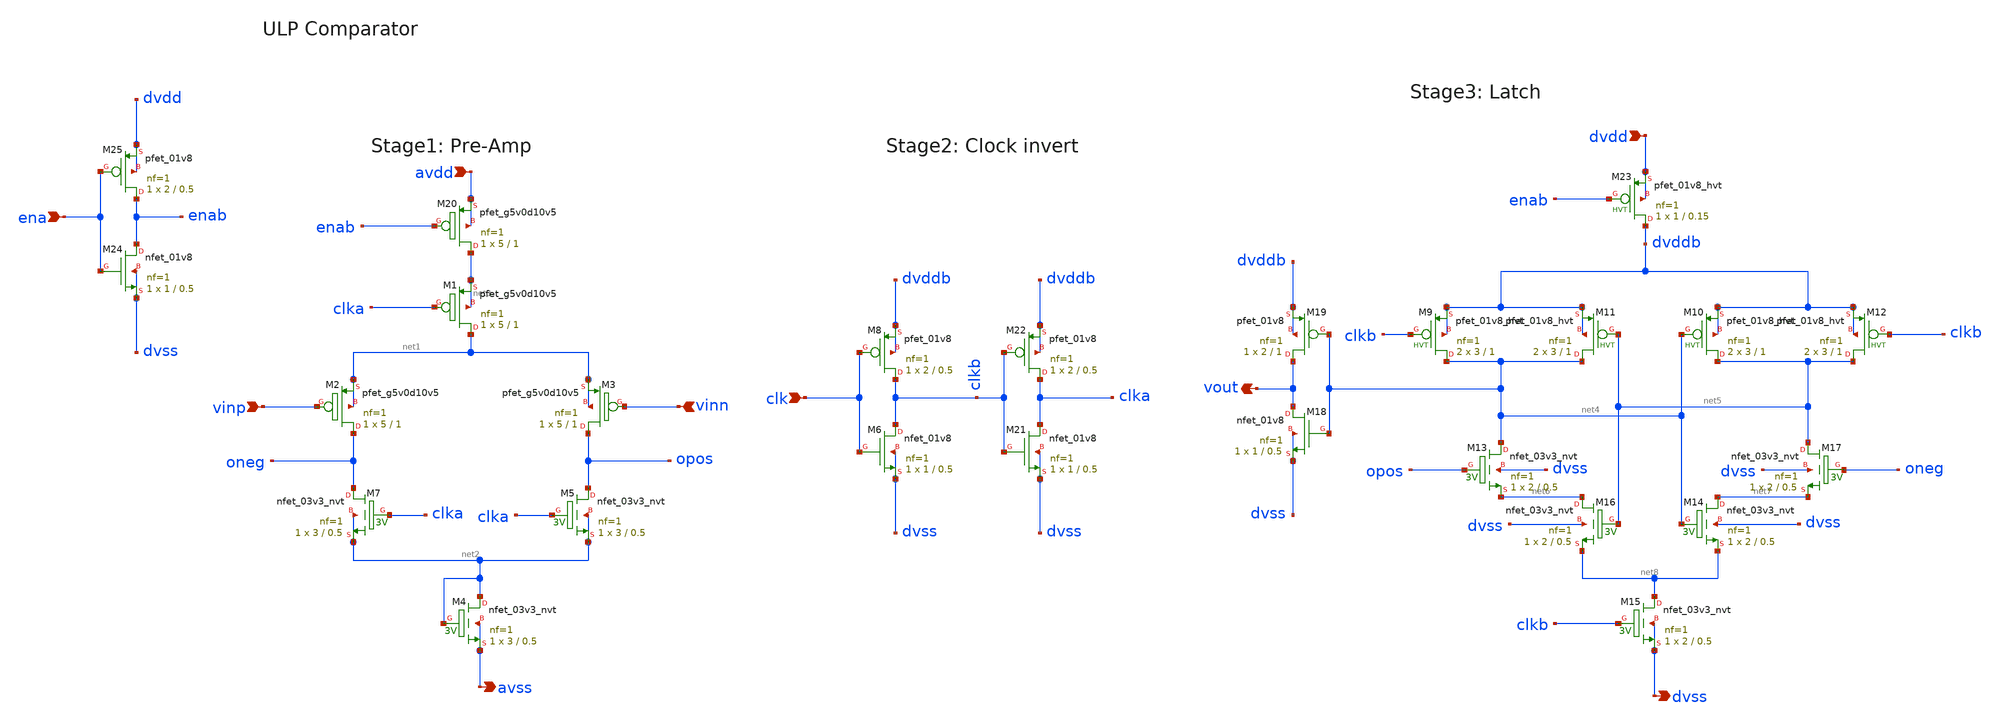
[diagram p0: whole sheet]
** sch_path: xschem/sky130_icrg_ip__ulpcomp2.sch
**.subckt sky130_icrg_ip__ulpcomp2 avdd vinp vinn avss vout dvss dvdd clk ena
*.ipin avdd
*.ipin vinp
*.ipin vinn
*.opin avss
*.opin vout
*.opin dvss
*.ipin dvdd
*.ipin clk
*.ipin ena
XM2 oneg vinp net1 net1 sky130_fd_pr__pfet_g5v0d10v5 L=1 W=5 nf=1 ad='int((nf+1)/2) * W/nf * 0.29' as='int((nf+2)/2) * W/nf * 0.29'
+ pd='2*int((nf+1)/2) * (W/nf + 0.29)' ps='2*int((nf+2)/2) * (W/nf + 0.29)' nrd='0.29 / W' nrs='0.29 / W'
+ sa=0 sb=0 sd=0 mult=1 m=1
XM3 opos vinn net1 net1 sky130_fd_pr__pfet_g5v0d10v5 L=1 W=5 nf=1 ad='int((nf+1)/2) * W/nf * 0.29' as='int((nf+2)/2) * W/nf * 0.29'
+ pd='2*int((nf+1)/2) * (W/nf + 0.29)' ps='2*int((nf+2)/2) * (W/nf + 0.29)' nrd='0.29 / W' nrs='0.29 / W'
+ sa=0 sb=0 sd=0 mult=1 m=1
XM7 oneg clka net2 net2 sky130_fd_pr__nfet_03v3_nvt L=0.5 W=3 nf=1 ad='int((nf+1)/2) * W/nf * 0.29' as='int((nf+2)/2) * W/nf * 0.29'
+ pd='2*int((nf+1)/2) * (W/nf + 0.29)' ps='2*int((nf+2)/2) * (W/nf + 0.29)' nrd='0.29 / W' nrs='0.29 / W'
+ sa=0 sb=0 sd=0 mult=1 m=1
XM5 opos clka net2 net2 sky130_fd_pr__nfet_03v3_nvt L=0.5 W=3 nf=1 ad='int((nf+1)/2) * W/nf * 0.29' as='int((nf+2)/2) * W/nf * 0.29'
+ pd='2*int((nf+1)/2) * (W/nf + 0.29)' ps='2*int((nf+2)/2) * (W/nf + 0.29)' nrd='0.29 / W' nrs='0.29 / W'
+ sa=0 sb=0 sd=0 mult=1 m=1
XM4 net2 net2 avss avss sky130_fd_pr__nfet_03v3_nvt L=0.5 W=3 nf=1 ad='int((nf+1)/2) * W/nf * 0.29' as='int((nf+2)/2) * W/nf * 0.29'
+ pd='2*int((nf+1)/2) * (W/nf + 0.29)' ps='2*int((nf+2)/2) * (W/nf + 0.29)' nrd='0.29 / W' nrs='0.29 / W'
+ sa=0 sb=0 sd=0 mult=1 m=1
XM18 vout net4 dvss dvss sky130_fd_pr__nfet_01v8 L=0.5 W=1 nf=1 ad='int((nf+1)/2) * W/nf * 0.29' as='int((nf+2)/2) * W/nf * 0.29'
+ pd='2*int((nf+1)/2) * (W/nf + 0.29)' ps='2*int((nf+2)/2) * (W/nf + 0.29)' nrd='0.29 / W' nrs='0.29 / W'
+ sa=0 sb=0 sd=0 mult=1 m=1
XM19 vout net4 dvddb dvddb sky130_fd_pr__pfet_01v8 L=1 W=2 nf=1 ad='int((nf+1)/2) * W/nf * 0.29' as='int((nf+2)/2) * W/nf * 0.29'
+ pd='2*int((nf+1)/2) * (W/nf + 0.29)' ps='2*int((nf+2)/2) * (W/nf + 0.29)' nrd='0.29 / W' nrs='0.29 / W'
+ sa=0 sb=0 sd=0 mult=1 m=1
XM22 clka clkb dvddb dvddb sky130_fd_pr__pfet_01v8 L=0.5 W=2 nf=1 ad='int((nf+1)/2) * W/nf * 0.29' as='int((nf+2)/2) * W/nf * 0.29'
+ pd='2*int((nf+1)/2) * (W/nf + 0.29)' ps='2*int((nf+2)/2) * (W/nf + 0.29)' nrd='0.29 / W' nrs='0.29 / W'
+ sa=0 sb=0 sd=0 mult=1 m=1
XM20 net3 enab avdd avdd sky130_fd_pr__pfet_g5v0d10v5 L=1 W=5 nf=1 ad='int((nf+1)/2) * W/nf * 0.29' as='int((nf+2)/2) * W/nf * 0.29'
+ pd='2*int((nf+1)/2) * (W/nf + 0.29)' ps='2*int((nf+2)/2) * (W/nf + 0.29)' nrd='0.29 / W' nrs='0.29 / W'
+ sa=0 sb=0 sd=0 mult=1 m=1
XM8 clkb clk dvddb dvddb sky130_fd_pr__pfet_01v8 L=0.5 W=2 nf=1 ad='int((nf+1)/2) * W/nf * 0.29' as='int((nf+2)/2) * W/nf * 0.29'
+ pd='2*int((nf+1)/2) * (W/nf + 0.29)' ps='2*int((nf+2)/2) * (W/nf + 0.29)' nrd='0.29 / W' nrs='0.29 / W'
+ sa=0 sb=0 sd=0 mult=1 m=1
XM25 enab ena dvdd dvdd sky130_fd_pr__pfet_01v8 L=0.5 W=2 nf=1 ad='int((nf+1)/2) * W/nf * 0.29' as='int((nf+2)/2) * W/nf * 0.29'
+ pd='2*int((nf+1)/2) * (W/nf + 0.29)' ps='2*int((nf+2)/2) * (W/nf + 0.29)' nrd='0.29 / W' nrs='0.29 / W'
+ sa=0 sb=0 sd=0 mult=1 m=1
XM13 net4 opos net6 dvss sky130_fd_pr__nfet_03v3_nvt L=0.5 W=2 nf=1 ad='int((nf+1)/2) * W/nf * 0.29'
+ as='int((nf+2)/2) * W/nf * 0.29' pd='2*int((nf+1)/2) * (W/nf + 0.29)' ps='2*int((nf+2)/2) * (W/nf + 0.29)'
+ nrd='0.29 / W' nrs='0.29 / W' sa=0 sb=0 sd=0 mult=1 m=1
XM14 net7 net4 net8 dvss sky130_fd_pr__nfet_03v3_nvt L=0.5 W=2 nf=1 ad='int((nf+1)/2) * W/nf * 0.29'
+ as='int((nf+2)/2) * W/nf * 0.29' pd='2*int((nf+1)/2) * (W/nf + 0.29)' ps='2*int((nf+2)/2) * (W/nf + 0.29)'
+ nrd='0.29 / W' nrs='0.29 / W' sa=0 sb=0 sd=0 mult=1 m=1
XM15 net8 clkb dvss dvss sky130_fd_pr__nfet_03v3_nvt L=0.5 W=2 nf=1 ad='int((nf+1)/2) * W/nf * 0.29'
+ as='int((nf+2)/2) * W/nf * 0.29' pd='2*int((nf+1)/2) * (W/nf + 0.29)' ps='2*int((nf+2)/2) * (W/nf + 0.29)'
+ nrd='0.29 / W' nrs='0.29 / W' sa=0 sb=0 sd=0 mult=1 m=1
XM16 net6 net5 net8 dvss sky130_fd_pr__nfet_03v3_nvt L=0.5 W=2 nf=1 ad='int((nf+1)/2) * W/nf * 0.29'
+ as='int((nf+2)/2) * W/nf * 0.29' pd='2*int((nf+1)/2) * (W/nf + 0.29)' ps='2*int((nf+2)/2) * (W/nf + 0.29)'
+ nrd='0.29 / W' nrs='0.29 / W' sa=0 sb=0 sd=0 mult=1 m=1
XM17 net5 oneg net7 dvss sky130_fd_pr__nfet_03v3_nvt L=0.5 W=2 nf=1 ad='int((nf+1)/2) * W/nf * 0.29'
+ as='int((nf+2)/2) * W/nf * 0.29' pd='2*int((nf+1)/2) * (W/nf + 0.29)' ps='2*int((nf+2)/2) * (W/nf + 0.29)'
+ nrd='0.29 / W' nrs='0.29 / W' sa=0 sb=0 sd=0 mult=1 m=1
XM6 clkb clk dvss dvss sky130_fd_pr__nfet_01v8 L=0.5 W=1 nf=1 ad='int((nf+1)/2) * W/nf * 0.29' as='int((nf+2)/2) * W/nf * 0.29'
+ pd='2*int((nf+1)/2) * (W/nf + 0.29)' ps='2*int((nf+2)/2) * (W/nf + 0.29)' nrd='0.29 / W' nrs='0.29 / W'
+ sa=0 sb=0 sd=0 mult=1 m=1
XM21 clka clkb dvss dvss sky130_fd_pr__nfet_01v8 L=0.5 W=1 nf=1 ad='int((nf+1)/2) * W/nf * 0.29' as='int((nf+2)/2) * W/nf * 0.29'
+ pd='2*int((nf+1)/2) * (W/nf + 0.29)' ps='2*int((nf+2)/2) * (W/nf + 0.29)' nrd='0.29 / W' nrs='0.29 / W'
+ sa=0 sb=0 sd=0 mult=1 m=1
XM24 enab ena dvss dvss sky130_fd_pr__nfet_01v8 L=0.5 W=1 nf=1 ad='int((nf+1)/2) * W/nf * 0.29' as='int((nf+2)/2) * W/nf * 0.29'
+ pd='2*int((nf+1)/2) * (W/nf + 0.29)' ps='2*int((nf+2)/2) * (W/nf + 0.29)' nrd='0.29 / W' nrs='0.29 / W'
+ sa=0 sb=0 sd=0 mult=1 m=1
XM1 net1 clka net3 net3 sky130_fd_pr__pfet_g5v0d10v5 L=1 W=5 nf=1 ad='int((nf+1)/2) * W/nf * 0.29' as='int((nf+2)/2) * W/nf * 0.29'
+ pd='2*int((nf+1)/2) * (W/nf + 0.29)' ps='2*int((nf+2)/2) * (W/nf + 0.29)' nrd='0.29 / W' nrs='0.29 / W'
+ sa=0 sb=0 sd=0 mult=1 m=1
XM23 dvddb enab dvdd dvdd sky130_fd_pr__pfet_01v8_hvt L=0.15 W=1 nf=1 ad='int((nf+1)/2) * W/nf * 0.29'
+ as='int((nf+2)/2) * W/nf * 0.29' pd='2*int((nf+1)/2) * (W/nf + 0.29)' ps='2*int((nf+2)/2) * (W/nf + 0.29)'
+ nrd='0.29 / W' nrs='0.29 / W' sa=0 sb=0 sd=0 mult=1 m=1
XM9 net4 clkb dvddb dvddb sky130_fd_pr__pfet_01v8_hvt L=1 W=3 nf=1 ad='int((nf+1)/2) * W/nf * 0.29' as='int((nf+2)/2) * W/nf * 0.29'
+ pd='2*int((nf+1)/2) * (W/nf + 0.29)' ps='2*int((nf+2)/2) * (W/nf + 0.29)' nrd='0.29 / W' nrs='0.29 / W'
+ sa=0 sb=0 sd=0 mult=2 m=2
XM10 net5 net4 dvddb dvddb sky130_fd_pr__pfet_01v8_hvt L=1 W=3 nf=1 ad='int((nf+1)/2) * W/nf * 0.29'
+ as='int((nf+2)/2) * W/nf * 0.29' pd='2*int((nf+1)/2) * (W/nf + 0.29)' ps='2*int((nf+2)/2) * (W/nf + 0.29)'
+ nrd='0.29 / W' nrs='0.29 / W' sa=0 sb=0 sd=0 mult=2 m=2
XM11 net4 net5 dvddb dvddb sky130_fd_pr__pfet_01v8_hvt L=1 W=3 nf=1 ad='int((nf+1)/2) * W/nf * 0.29'
+ as='int((nf+2)/2) * W/nf * 0.29' pd='2*int((nf+1)/2) * (W/nf + 0.29)' ps='2*int((nf+2)/2) * (W/nf + 0.29)'
+ nrd='0.29 / W' nrs='0.29 / W' sa=0 sb=0 sd=0 mult=2 m=2
XM12 net5 clkb dvddb dvddb sky130_fd_pr__pfet_01v8_hvt L=1 W=3 nf=1 ad='int((nf+1)/2) * W/nf * 0.29'
+ as='int((nf+2)/2) * W/nf * 0.29' pd='2*int((nf+1)/2) * (W/nf + 0.29)' ps='2*int((nf+2)/2) * (W/nf + 0.29)'
+ nrd='0.29 / W' nrs='0.29 / W' sa=0 sb=0 sd=0 mult=2 m=2
**.ends
.end
